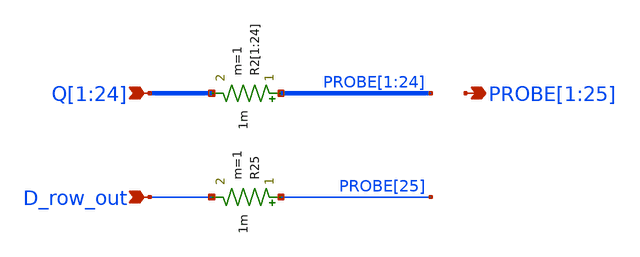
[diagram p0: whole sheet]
** sch_path: probe_connector_25/probe_connector_25.sch
**.subckt probe_connector_25
*+ PROBE[1],PROBE[2],PROBE[3],PROBE[4],PROBE[5],PROBE[6],PROBE[7],PROBE[8],PROBE[9],PROBE[10],PROBE[11],PROBE[12],PROBE[13],PROBE[14],PROBE[15],PROBE[16],PROBE[17],PROBE[18],PROBE[19],PROBE[20],PROBE[21],PROBE[22],PROBE[23],PROBE[24],PROBE[25]
*+ Q[1],Q[2],Q[3],Q[4],Q[5],Q[6],Q[7],Q[8],Q[9],Q[10],Q[11],Q[12],Q[13],Q[14],Q[15],Q[16],Q[17],Q[18],Q[19],Q[20],Q[21],Q[22],Q[23],Q[24] D_row_out
*.opin
*+ PROBE[1],PROBE[2],PROBE[3],PROBE[4],PROBE[5],PROBE[6],PROBE[7],PROBE[8],PROBE[9],PROBE[10],PROBE[11],PROBE[12],PROBE[13],PROBE[14],PROBE[15],PROBE[16],PROBE[17],PROBE[18],PROBE[19],PROBE[20],PROBE[21],PROBE[22],PROBE[23],PROBE[24],PROBE[25]
*.ipin
*+ Q[1],Q[2],Q[3],Q[4],Q[5],Q[6],Q[7],Q[8],Q[9],Q[10],Q[11],Q[12],Q[13],Q[14],Q[15],Q[16],Q[17],Q[18],Q[19],Q[20],Q[21],Q[22],Q[23],Q[24]
*.ipin D_row_out
R25 PROBE[25] D_row_out 1m m=1
R2[1] PROBE[1] Q[1] 1m m=1
R2[2] PROBE[2] Q[2] 1m m=1
R2[3] PROBE[3] Q[3] 1m m=1
R2[4] PROBE[4] Q[4] 1m m=1
R2[5] PROBE[5] Q[5] 1m m=1
R2[6] PROBE[6] Q[6] 1m m=1
R2[7] PROBE[7] Q[7] 1m m=1
R2[8] PROBE[8] Q[8] 1m m=1
R2[9] PROBE[9] Q[9] 1m m=1
R2[10] PROBE[10] Q[10] 1m m=1
R2[11] PROBE[11] Q[11] 1m m=1
R2[12] PROBE[12] Q[12] 1m m=1
R2[13] PROBE[13] Q[13] 1m m=1
R2[14] PROBE[14] Q[14] 1m m=1
R2[15] PROBE[15] Q[15] 1m m=1
R2[16] PROBE[16] Q[16] 1m m=1
R2[17] PROBE[17] Q[17] 1m m=1
R2[18] PROBE[18] Q[18] 1m m=1
R2[19] PROBE[19] Q[19] 1m m=1
R2[20] PROBE[20] Q[20] 1m m=1
R2[21] PROBE[21] Q[21] 1m m=1
R2[22] PROBE[22] Q[22] 1m m=1
R2[23] PROBE[23] Q[23] 1m m=1
R2[24] PROBE[24] Q[24] 1m m=1
**.ends
.end
